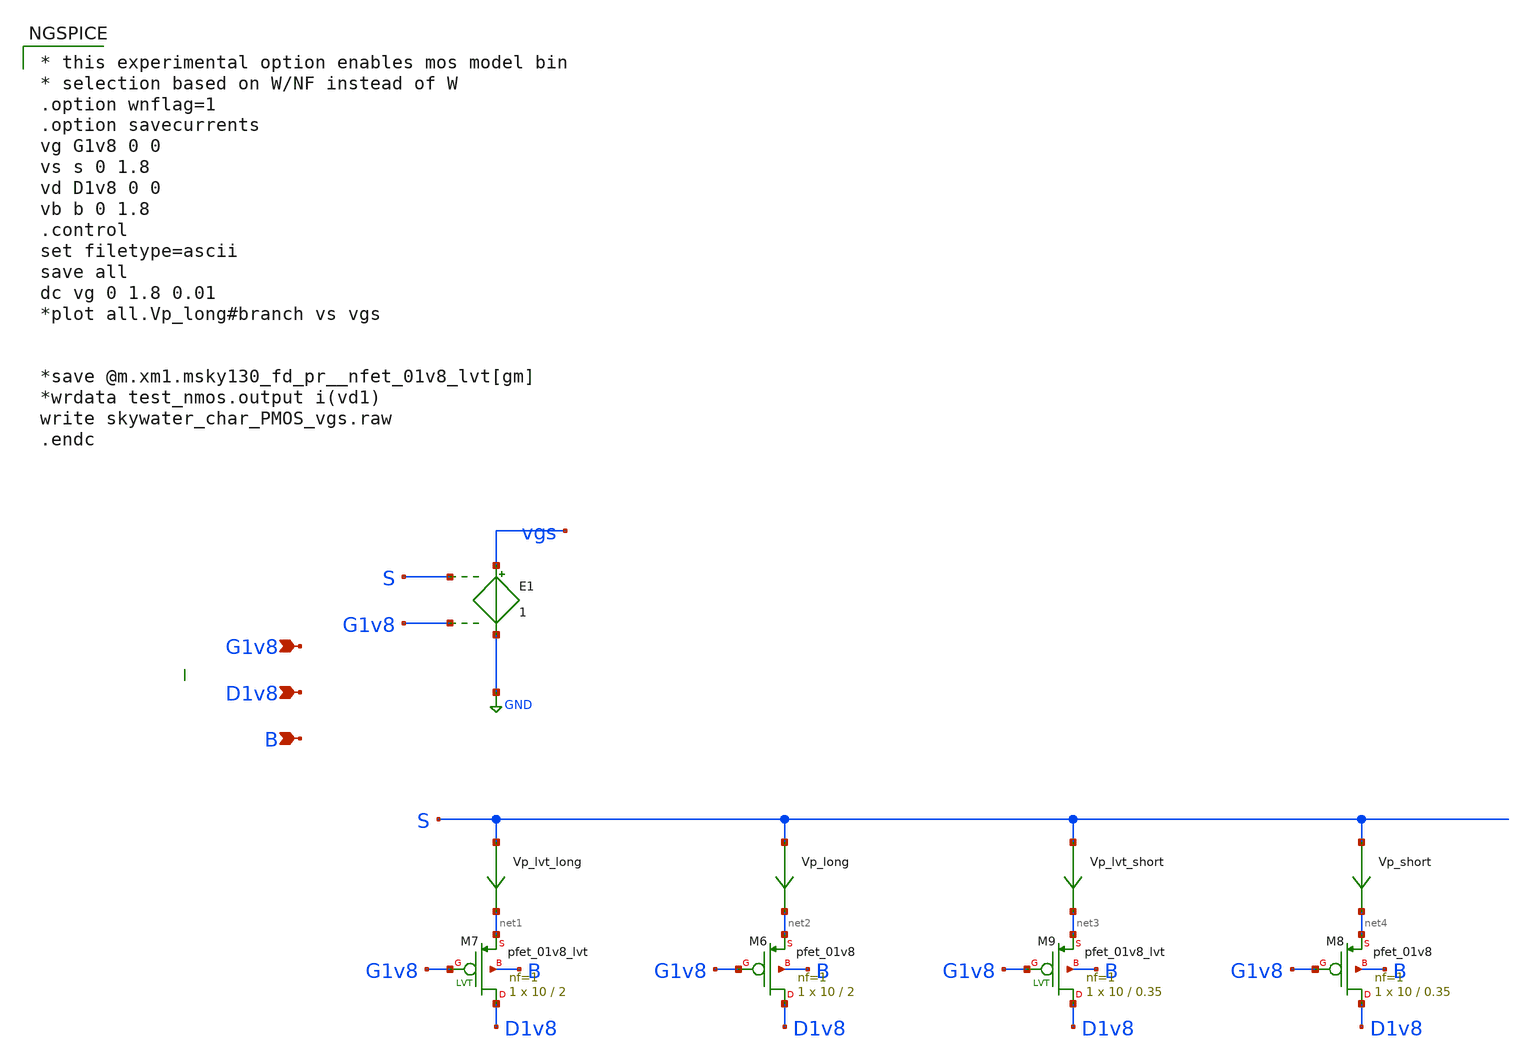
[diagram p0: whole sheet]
** sch_path: src/iCHIP/resources/char_schem_PMOS_vgs.sch
* Copyright 2020 Stefan Frederik Schippers
* Licensed under the Apache License, Version 2.0 (the "License");
* you may not use this file except in compliance with the License.
* You may obtain a copy of the License at
* https://www.apache.org/licenses/LICENSE-2.0
* Unless required by applicable law or agreed to in writing, software
* distributed under the License is distributed on an "AS IS" BASIS,
* WITHOUT WARRANTIES OR CONDITIONS OF ANY KIND, either express or implied.
* See the License for the specific language governing permissions and
* limitations under the License.
**.subckt char_schem_PMOS_vgs G1v8 D1v8 B
*.ipin G1v8
*.ipin D1v8
*.ipin B
Vp_lvt_long S net1 0
.save i(vp_lvt_long)
Vp_long S net2 0
.save i(vp_long)
Vp_lvt_short S net3 0
.save i(vp_lvt_short)
Vp_short S net4 0
.save i(vp_short)
XM6 D1v8 G1v8 net2 B sky130_fd_pr__pfet_01v8 L=2 W=10 nf=1 ad='int((nf+1)/2) * W/nf * 0.29' as='int((nf+2)/2) * W/nf * 0.29'
+ pd='2*int((nf+1)/2) * (W/nf + 0.29)' ps='2*int((nf+2)/2) * (W/nf + 0.29)' nrd='0.29 / W' nrs='0.29 / W'
+ sa=0 sb=0 sd=0 mult=1 m=1
XM7 D1v8 G1v8 net1 B sky130_fd_pr__pfet_01v8_lvt L=2 W=10 nf=1 ad='int((nf+1)/2) * W/nf * 0.29' as='int((nf+2)/2) * W/nf * 0.29'
+ pd='2*int((nf+1)/2) * (W/nf + 0.29)' ps='2*int((nf+2)/2) * (W/nf + 0.29)' nrd='0.29 / W' nrs='0.29 / W'
+ sa=0 sb=0 sd=0 mult=1 m=1
XM8 D1v8 G1v8 net4 B sky130_fd_pr__pfet_01v8 L=0.35 W=10 nf=1 ad='int((nf+1)/2) * W/nf * 0.29' as='int((nf+2)/2) * W/nf * 0.29'
+ pd='2*int((nf+1)/2) * (W/nf + 0.29)' ps='2*int((nf+2)/2) * (W/nf + 0.29)' nrd='0.29 / W' nrs='0.29 / W'
+ sa=0 sb=0 sd=0 mult=1 m=1
XM9 D1v8 G1v8 net3 B sky130_fd_pr__pfet_01v8_lvt L=0.35 W=10 nf=1 ad='int((nf+1)/2) * W/nf * 0.29' as='int((nf+2)/2) * W/nf * 0.29'
+ pd='2*int((nf+1)/2) * (W/nf + 0.29)' ps='2*int((nf+2)/2) * (W/nf + 0.29)' nrd='0.29 / W' nrs='0.29 / W'
+ sa=0 sb=0 sd=0 mult=1 m=1
E1 vgs GND S G1v8 1
**** begin user architecture code

.include $::SKYWATER_MODELS/cells/nfet_01v8/sky130_fd_pr__nfet_01v8__tt.corner.spice
.include $::SKYWATER_MODELS/cells/nfet_01v8_lvt/sky130_fd_pr__nfet_01v8_lvt__tt.corner.spice
.include $::SKYWATER_MODELS/cells/pfet_01v8/sky130_fd_pr__pfet_01v8__tt.corner.spice
.include $::SKYWATER_MODELS/cells/nfet_03v3_nvt/sky130_fd_pr__nfet_03v3_nvt__tt.corner.spice
.include $::SKYWATER_MODELS/cells/nfet_05v0_nvt/sky130_fd_pr__nfet_05v0_nvt__tt.corner.spice
.include $::SKYWATER_MODELS/cells/esd_nfet_01v8/sky130_fd_pr__esd_nfet_01v8__tt.corner.spice
.include $::SKYWATER_MODELS/cells/pfet_01v8_lvt/sky130_fd_pr__pfet_01v8_lvt__tt.corner.spice
.include $::SKYWATER_MODELS/cells/pfet_01v8_hvt/sky130_fd_pr__pfet_01v8_hvt__tt.corner.spice
.include $::SKYWATER_MODELS/cells/esd_pfet_g5v0d10v5/sky130_fd_pr__esd_pfet_g5v0d10v5__tt.corner.spice
.include $::SKYWATER_MODELS/cells/pfet_g5v0d10v5/sky130_fd_pr__pfet_g5v0d10v5__tt.corner.spice
.include $::SKYWATER_MODELS/cells/pfet_g5v0d16v0/sky130_fd_pr__pfet_g5v0d16v0__tt.corner.spice
.include $::SKYWATER_MODELS/cells/nfet_g5v0d10v5/sky130_fd_pr__nfet_g5v0d10v5__tt.corner.spice
.include $::SKYWATER_MODELS/cells/nfet_g5v0d16v0/sky130_fd_pr__nfet_g5v0d16v0__tt_discrete.corner.spice
.include $::SKYWATER_MODELS/cells/esd_nfet_g5v0d10v5/sky130_fd_pr__esd_nfet_g5v0d10v5__tt.corner.spice
.include $::SKYWATER_MODELS/models/corners/tt/nonfet.spice
* Mismatch parameters
.include $::SKYWATER_MODELS/cells/nfet_01v8/sky130_fd_pr__nfet_01v8__mismatch.corner.spice
.include $::SKYWATER_MODELS/cells/pfet_01v8/sky130_fd_pr__pfet_01v8__mismatch.corner.spice
.include $::SKYWATER_MODELS/cells/nfet_01v8_lvt/sky130_fd_pr__nfet_01v8_lvt__mismatch.corner.spice
.include $::SKYWATER_MODELS/cells/pfet_01v8_lvt/sky130_fd_pr__pfet_01v8_lvt__mismatch.corner.spice
.include $::SKYWATER_MODELS/cells/pfet_01v8_hvt/sky130_fd_pr__pfet_01v8_hvt__mismatch.corner.spice
.include $::SKYWATER_MODELS/cells/nfet_g5v0d10v5/sky130_fd_pr__nfet_g5v0d10v5__mismatch.corner.spice
.include $::SKYWATER_MODELS/cells/pfet_g5v0d10v5/sky130_fd_pr__pfet_g5v0d10v5__mismatch.corner.spice
.include $::SKYWATER_MODELS/cells/nfet_05v0_nvt/sky130_fd_pr__nfet_05v0_nvt__mismatch.corner.spice
.include $::SKYWATER_MODELS/cells/nfet_03v3_nvt/sky130_fd_pr__nfet_03v3_nvt__mismatch.corner.spice
* Resistor$::SKYWATER_MODELS/Capacitor
.include $::SKYWATER_MODELS/models/r+c/res_typical__cap_typical.spice
.include $::SKYWATER_MODELS/models/r+c/res_typical__cap_typical__lin.spice
* Special cells
.include $::SKYWATER_MODELS/models/corners/tt/specialized_cells.spice
* All models
.include $::SKYWATER_MODELS/models/all.spice
* Corner
.include $::SKYWATER_MODELS/models/corners/tt/rf.spice


* this experimental option enables mos model bin
* selection based on W/NF instead of W
.option wnflag=1
.option savecurrents
vg G1v8 0 0
vs s 0 1.8
vd D1v8 0 0
vb b 0 1.8
.control
set filetype=ascii
save all
dc vg 0 1.8 0.01
*plot all.Vp_long#branch vs vgs


*save @m.xm1.msky130_fd_pr__nfet_01v8_lvt[gm]
*wrdata test_nmos.output i(vd1)
write skywater_char_PMOS_vgs.raw
.endc



.include $::SKYWATER_MODELS/cells/nfet_20v0/sky130_fd_pr__nfet_20v0__tt_discrete.corner.spice

**** end user architecture code
**.ends
.GLOBAL GND
.end
